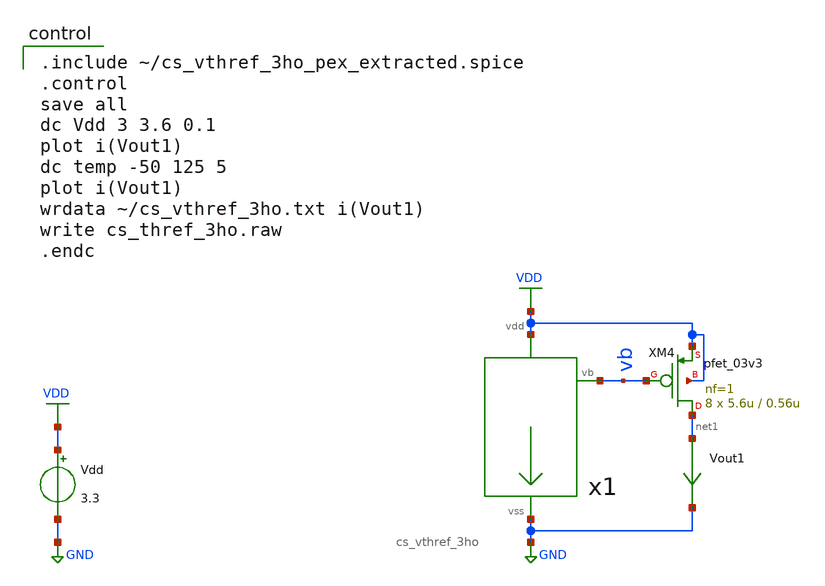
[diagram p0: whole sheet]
** sch_path: CS/tbdc_cs_vthref_pex_3ho.sch
**.subckt tbdc_cs_vthref_pex_3ho
Vdd VDD GND 3.3
XM4 net1 vb VDD VDD pfet_03v3 L=0.56u W=5.6u nf=1 ad='int((nf+1)/2) * W/nf * 0.18u' as='int((nf+2)/2) * W/nf * 0.18u'
+ pd='2*int((nf+1)/2) * (W/nf + 0.18u)' ps='2*int((nf+2)/2) * (W/nf + 0.18u)' nrd='0.18u / W' nrs='0.18u / W'
+ sa=0 sb=0 sd=0 m=8
Vout1 net1 GND 0
.save i(vout1)
x1 GND VDD vb cs_vthref_3ho
**** begin user architecture code

.include $::180MCU_MODELS/design.ngspice
.lib $::180MCU_MODELS/sm141064.ngspice typical
.lib $::180MCU_MODELS/sm141064.ngspice res_typical
.lib $::180MCU_MODELS/sm141064.ngspice moscap_typical
.lib $::180MCU_MODELS/sm141064.ngspice bjt_typical
* .lib $::180MCU_MODELS/sm141064.ngspice res_statistical


.include ~/cs_vthref_3ho_pex_extracted.spice
.control
save all
dc Vdd 3 3.6 0.1
plot i(Vout1)
dc temp -50 125 5
plot i(Vout1)
wrdata ~/cs_vthref_3ho.txt i(Vout1)
write cs_thref_3ho.raw
.endc

**** end user architecture code
**.ends
.GLOBAL GND
.GLOBAL VDD
.end
